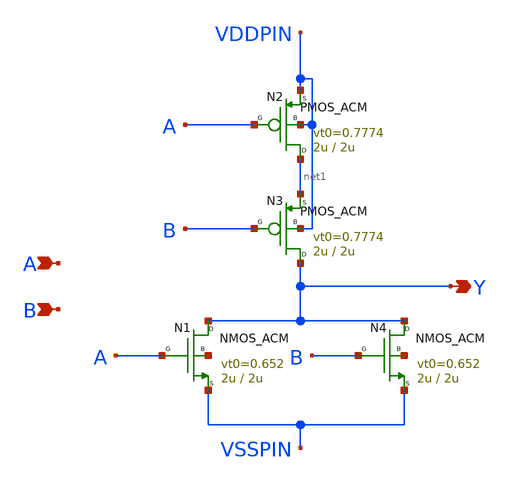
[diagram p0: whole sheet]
** sch_path: legacy/Examples/IHP-SG13/xschem/symbol/nor2_acm.sch
**.subckt nor2_acm A Y B
*.ipin A
*.opin Y
*.ipin B
N1 Y A VSSPIN net2 NMOS_ACM w=2u l=2u n=1.38 is=67.3n vt0=0.652 sigma=20m zeta=5m
N2 net1 A VDDPIN VDDPIN PMOS_ACM w=2u l=2u n=1.438 is=17.94n vt0=0.7774 sigma=20m zeta=5m
N3 Y B net1 VDDPIN PMOS_ACM w=2u l=2u n=1.438 is=17.94n vt0=0.7774 sigma=20m zeta=5m
N4 Y B VSSPIN net3 NMOS_ACM w=2u l=2u n=1.38 is=67.3n vt0=0.652 sigma=20m zeta=5m
**.ends
.end
